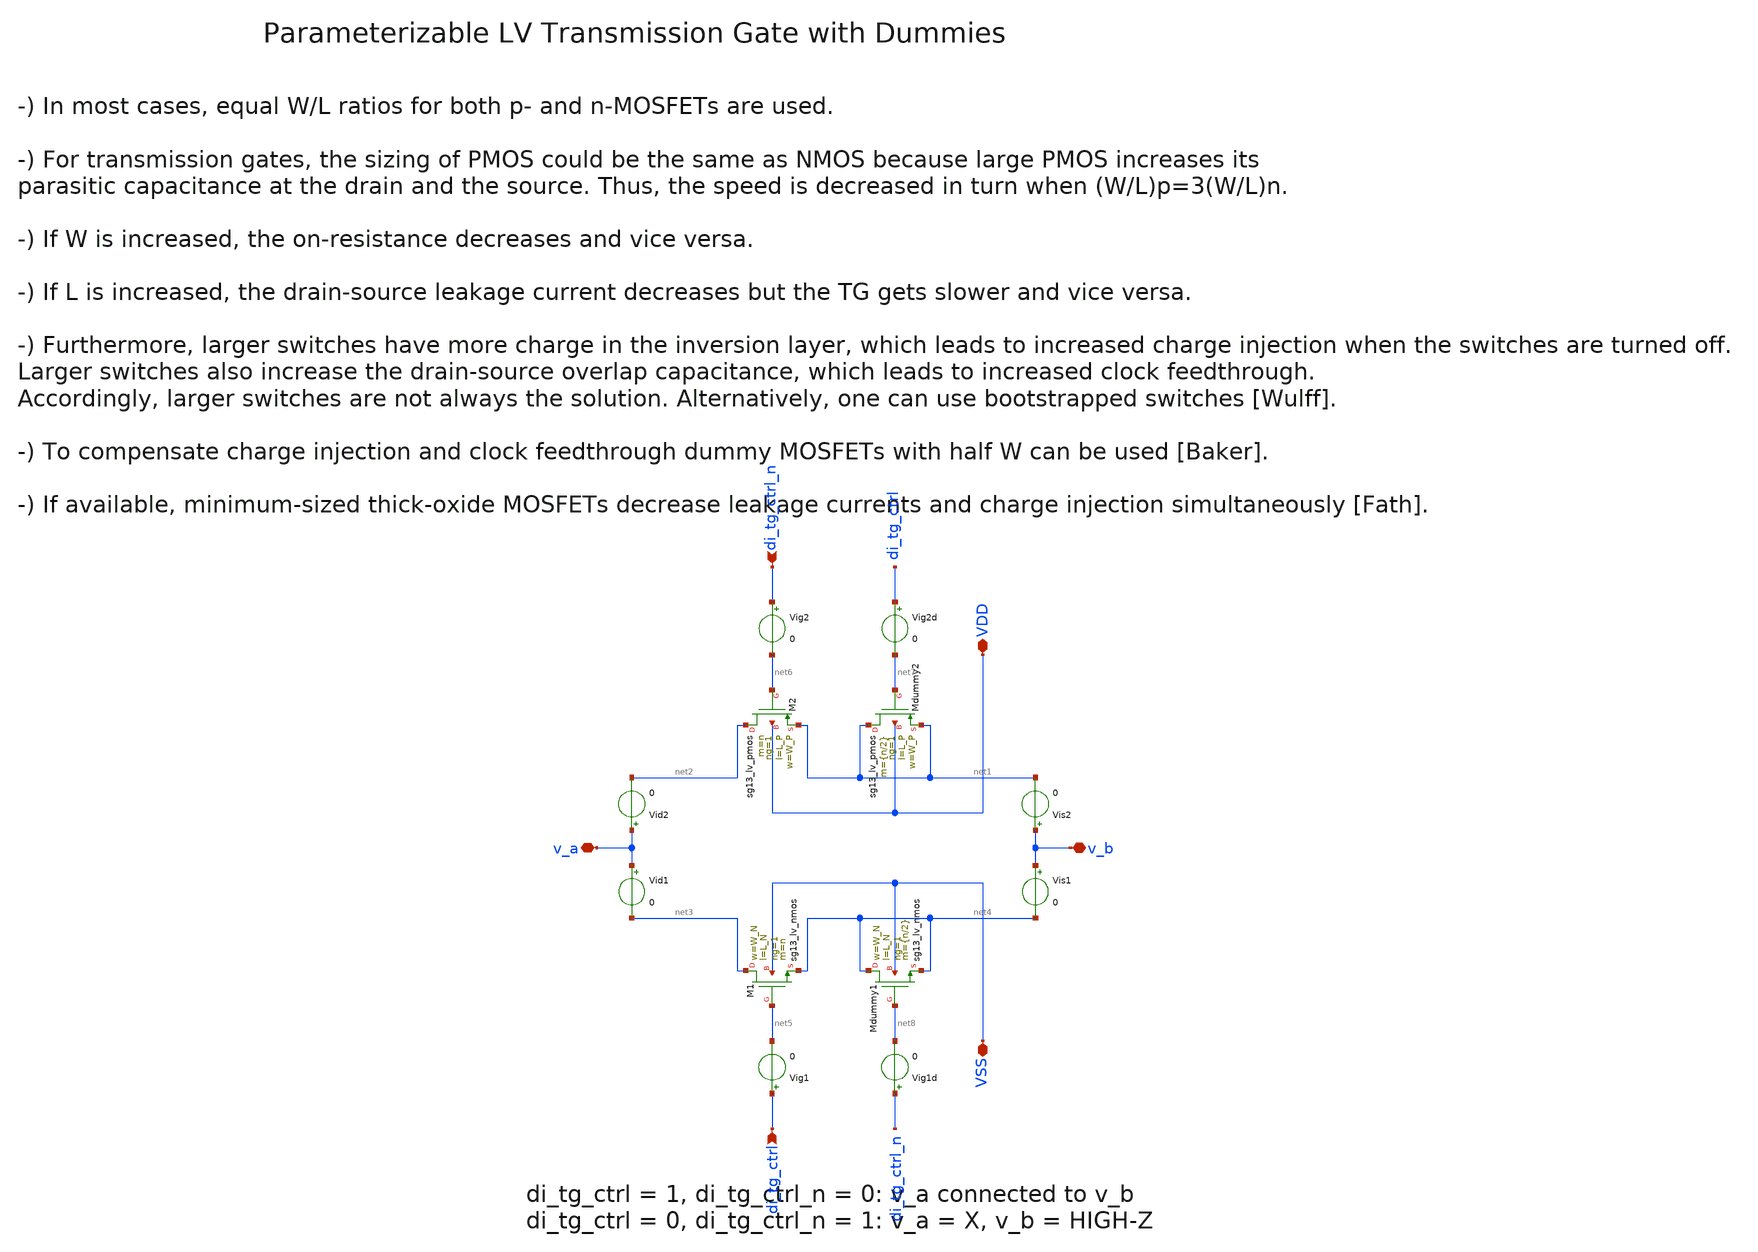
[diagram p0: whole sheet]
** sch_path: xschem/transmission_gate/transmission_gate_lv_w_dummy.sch
**.subckt transmission_gate_lv_w_dummy v_a v_b VDD VSS di_tg_ctrl di_tg_ctrl_n
*.iopin v_a
*.iopin v_b
*.iopin VDD
*.iopin VSS
*.ipin di_tg_ctrl
*.ipin di_tg_ctrl_n
XM1 net3 net5 net4 VSS sg13_lv_nmos w=W_N l=L_N ng=1 m=n mm_ok=1
XM2 net2 net6 net1 VDD sg13_lv_pmos w=W_P l=L_P ng=1 m=n mm_ok=1
XMdummy2 net1 net7 net1 VDD sg13_lv_pmos w=W_P l=L_P ng=1 m={n/2} mm_ok=1
XMdummy1 net4 net8 net4 VSS sg13_lv_nmos w=W_N l=L_N ng=1 m={n/2} mm_ok=1
Vig1 di_tg_ctrl net5 0
Vig2 di_tg_ctrl_n net6 0
Vig1d di_tg_ctrl_n net8 0
Vig2d di_tg_ctrl net7 0
Vid2 v_a net2 0
Vid1 v_a net3 0
Vis2 v_b net1 0
Vis1 v_b net4 0
**.ends
.end
